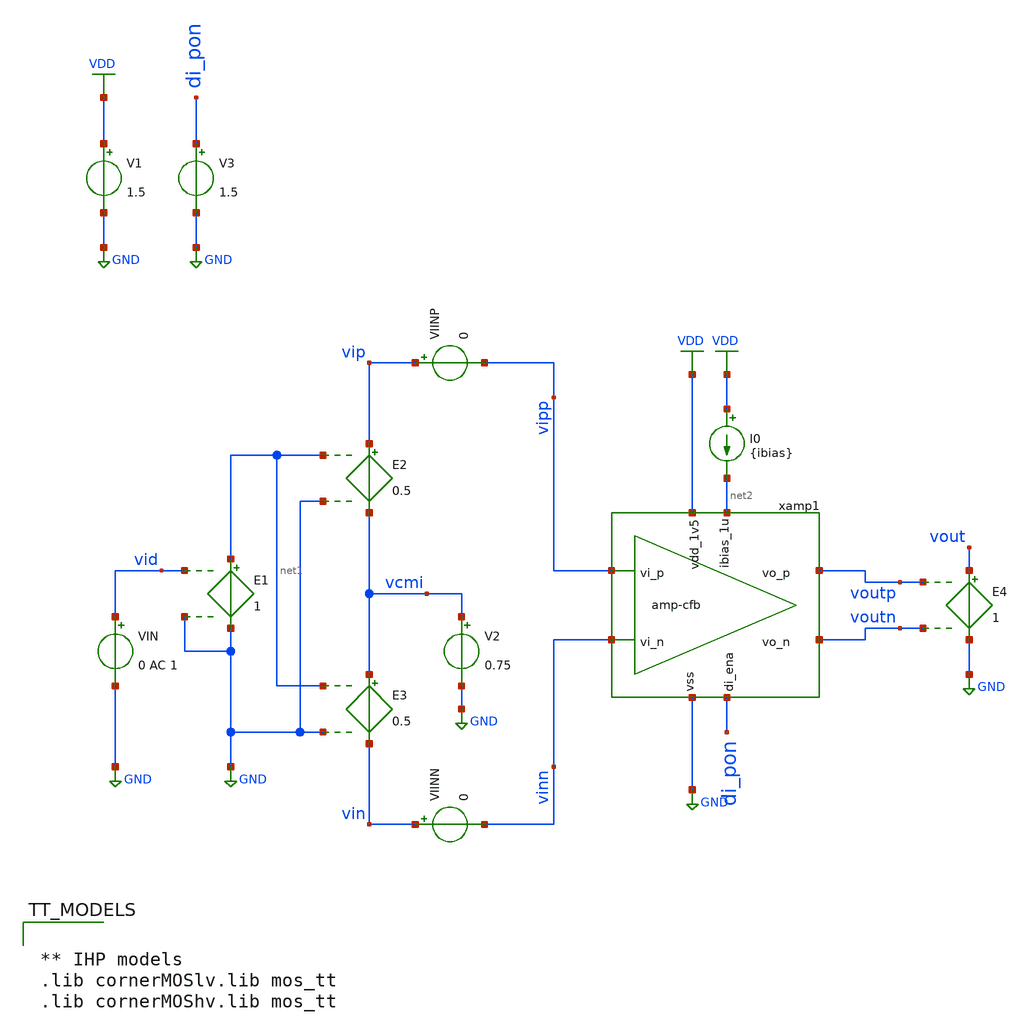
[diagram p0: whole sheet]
** sch_path: xschem/legacy/amp-cfb_tb-tran.sch
* xschem/ota-5t-fd.sch:
* (c) 2025 M. Koefinger
**.subckt amp-cfb_tb-tran
V1 VDD GND 1.5
V3 di_pon GND 1.5
V2 vcmi GND 0.75
E3 vcmi vin net1 GND 0.5
E2 vip vcmi net1 GND 0.5
VIN vid GND 0 AC 1
E1 net1 GND vid GND 1
VIINP vip vipp 0
VIINN vin vinn 0
xamp1 VDD net2 vipp voutp voutn vinn di_pon GND amp-cfb
I0 VDD net2 {ibias}
E4 vout GND voutp voutn 1
**** begin user architecture code


.include amp-cfb_tb-tran.save
*.include ../xschem/ota-5t-fd-dev-sav.spice
.options savecurrents
.options method=gear reltol=.005
.options sparse
.param ibias=20u
.param gain_cl=1
.param ci=100f
.param cfb=ci
.param cl=2*ci
.param Rfb=100M
.param Ri=Rfb
.ic v(xamp1.vgndp)=0.75 v(xamp1.vgndn)=0.75
.control
save all

let f_min = 10
let f_max = 1G
let f_stop = 500k

let Adc = 1
let err_gain_spec = 0.25
let v_step_o = 1.5
let v_step_i = v_step_o/Adc

let n_per_startup = 10
let fs = 100Meg
let tsettle = 1/fs/2
let t_rf = 0.1p
let t_on = tsettle/2
let t_delay = n_per_startup*tsettle
let t_per = tsettle

let tstep = 0.1*t_rf
let tstop = 10*t_per+t_delay
let tstart = t_delay

alter @VIN[DC] = 0.0

set wr_singlescale
set wr_vecnames
option numdgt=3

set opSimOnly = 0

** Main Simulations
if $opSimOnly eq 0
	op
	alter @VIN[PULSE] = [ 0 $&v_step_i $&t_delay $&t_rf $&t_rf $&t_on $&t_per 0 ]
	optran 0 0 0 1u 10m 0
	tran $&tstep $&tstop $&tstart

	setplot tran1
	let vid = v(vid)
	let iop = viop#branch
	let ion = vion#branch
	let vcmo = (voutp+voutn)/2
	let phi1 = v(xamp1.vphi1)
	let phi2 = v(xamp1.vphi2)
	plot phi1 phi2

	*plot iop ion
	plot vid vout vcmo
	plot v(vip) v(vin) v(voutp) v(voutn) vcmo

end

alter @VIN[DC] = 0
op
remzerovec
write ota-5t-fd_tb-cl.raw
.endc



** IHP models
.lib cornerMOSlv.lib mos_tt
.lib cornerMOShv.lib mos_tt


**** end user architecture code
**.ends

* expanding   symbol:  amp-cfb.sym # of pins=8
** sym_path: xschem/amp-cfb.sym
** sch_path: xschem/amp-cfb.sch
.subckt amp-cfb vdd_1v5 ibias_1u vi_p vo_p vo_n vi_n di_ena vss
*.ipin vi_p
*.ipin vi_n
*.ipin di_ena
*.iopin vss
*.iopin vdd_1v5
*.ipin ibias_1u
*.opin vo_n
*.opin vo_p
C1 vi_p vgndn 100f m=1
C2 vo_p vgndn 100f m=1
C3 vo_p vss 100f m=1
C4 vi_n vgndp 100f m=1
C5 vgndp vo_n 100f m=1
C6 vo_n vss 100f m=1
xamp1 vdd_1v5 vfb vo_p vo_n vgndp vgndn ibias_1u di_ena vss net1 ota-5t-fd
xcmfb1 vphi1 vphi2 vss vo_p vcm net1 vfb vo_n cmfb_sc cap=100f div=10
xclkgen1 vphi1 vphi2 vss clk_noverlap_ideal fs=100Meg tnover=2n tdelay=0 trf=0.1n
V1 vcm vss 0.75
.ends


* expanding   symbol:  ota-5t-fd.sym # of pins=10
** sym_path: xschem/ota-5t-fd.sym
** sch_path: xschem/ota-5t-fd.sch
.subckt ota-5t-fd vdd vfb voutp voutn vinp vinn ibias_1u5 d_ena vss vbp
*.ipin ibias_1u5
*.iopin vdd
*.iopin vss
*.ipin vinp
*.ipin vinn
*.opin voutn
*.ipin d_ena
*.opin voutp
*.ipin vfb
*.opin vbp
XMN3 tail gate_n vss vss sg13_lv_nmos w=2.5u l=0.5u ng=5 m=1 mm_ok=1
XMP2 voutp vfb vdd vdd sg13_lv_pmos w=0.5u l=0.5u ng=1 m=1 mm_ok=1
XMN1 voutn vinp tail vss sg13_lv_nmos w=5.5u l=0.5u ng=11 m=1 mm_ok=1
XMN2 voutp vinn tail vss sg13_lv_nmos w=5.5u l=0.5u ng=11 m=1 mm_ok=1
XMP1 voutn vfb vdd vdd sg13_lv_pmos w=0.5u l=0.5u ng=1 m=1 mm_ok=1
XMN4 ibias_1u5 gate_n vss vss sg13_lv_nmos w=1.5u l=0.5u ng=3 m=1 mm_ok=1
XMN5 gate_n ena_n vss vss sg13_lv_nmos w=0.5u l=0.13u ng=1 m=1 mm_ok=1
XMPSW1 vfb ena vdd vdd sg13_lv_pmos w=1.5u l=0.13u ng=1 m=1 mm_ok=1
XMN8 ena ena_n vss vss sg13_lv_nmos w=0.5u l=0.13u ng=1 m=1 mm_ok=1
XMP5 ena ena_n vdd vdd sg13_lv_pmos w=1.5u l=0.13u ng=1 m=1 mm_ok=1
XMN6 ibias_1u5 ena gate_n vss sg13_lv_nmos w=0.5u l=0.13u ng=1 m=1 mm_ok=1
XMN7 ena_n d_ena vss vss sg13_lv_nmos w=0.5u l=0.13u ng=1 m=1 mm_ok=1
XMP4 ena_n d_ena vdd vdd sg13_lv_pmos w=1.5u l=0.13u ng=1 m=1 mm_ok=1
XMN9 vbp gate_n vss vss sg13_lv_nmos w=1u l=0.5u ng=2 m=1 mm_ok=1
XMP3 vbp vbp vdd vdd sg13_lv_pmos w=0.5u l=0.5u ng=1 m=1 mm_ok=1
.ends


* expanding   symbol:  cmfb_sc.sym # of pins=8
** sym_path: xschem/cmfb_sc.sym
** sch_path: xschem/cmfb_sc.sch
.subckt cmfb_sc vphi2 vphi1 vss vo_p vcm vbias vfb vo_n  cap=100f div=10
*.ipin vcm
*.ipin vphi2
*.ipin vphi1
*.iopin vss
*.ipin vbias
*.iopin vo_p
*.iopin vo_n
*.opin vfb
C1 vo_p vfb 100f m=1
C2 net1 net2 10f m=1
C3 vfb vo_n 100f m=1
C4 net2 net3 10f m=1
S3 net1 vo_p vphi1 vss SW1
S4 vcm net1 vphi2 vss SW1
S6 net2 vfb vphi1 vss SW1
S7 vbias net2 vphi2 vss SW1
S9 net3 vo_n vphi1 vss SW1
S10 vcm net3 vphi2 vss SW1
.ends


* expanding   symbol:  clk_noverlap_ideal.sym # of pins=3
** sym_path: xschem/clk_noverlap_ideal.sym
** sch_path: xschem/clk_noverlap_ideal.sch
.subckt clk_noverlap_ideal vphi1 vphi2 vss  fs=100Meg tnover=2n tdelay=0 trf=0.1n
*.iopin vss
*.opin vphi1
*.opin vphi2
V1 vphi1 vss 0 PULSE 0 1.5 {tdelay} {trf} {trf} {0.5/{fs}-{tnover}} {1/{fs}} 0
V2 vphi2 vss 0 PULSE 0 1.5 {{tdelay}+{0.5/{fs}}} {trf} {trf} {0.5/{fs}-{tnover}} {1/{fs}} 0
.ends

.GLOBAL GND
.GLOBAL VDD
**** begin user architecture code
.MODEL SW1 SW( VT=0.75 VH=0.01 RON=1 ROFF=1G )
**** end user architecture code
.end
